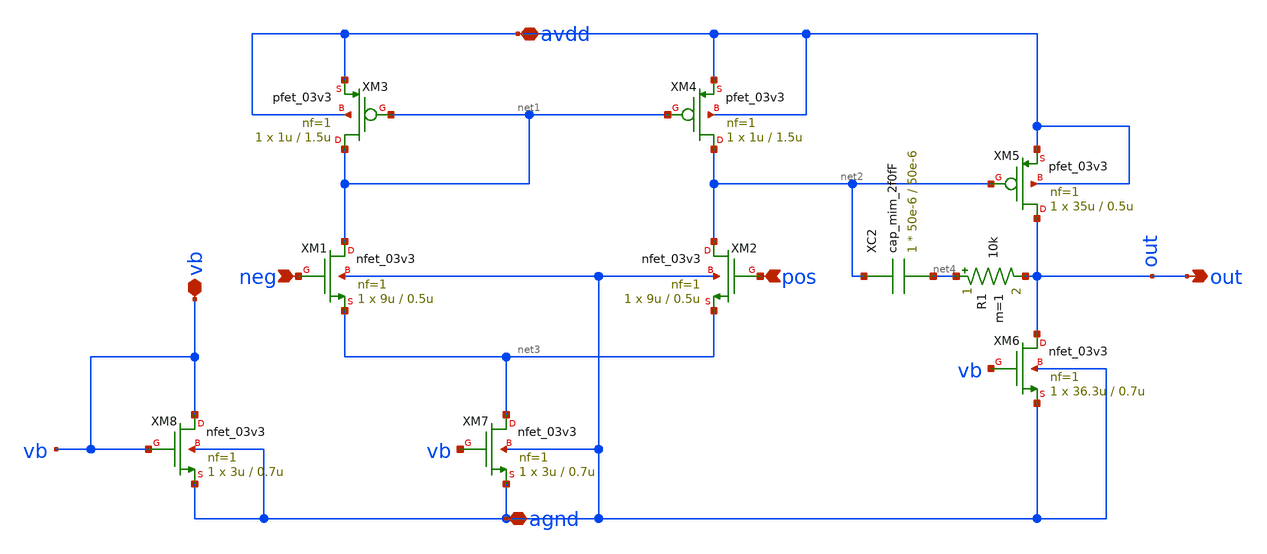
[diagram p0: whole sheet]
** sch_path: LDO/xschem/ota-ldo/symbol/ota-ldo.sch
**.subckt ota-ldo vb avdd agnd neg pos out
*.iopin vb
*.iopin avdd
*.iopin agnd
*.ipin neg
*.ipin pos
*.opin out
XC2 net2 net4 cap_mim_2f0fF c_width=50e-6 c_length=50e-6 m=1
XM1 net1 neg net3 agnd nfet_03v3 L=0.5u W=9u nf=1 ad='int((nf+1)/2) * W/nf * 0.18u' as='int((nf+2)/2) * W/nf * 0.18u'
+ pd='2*int((nf+1)/2) * (W/nf + 0.18u)' ps='2*int((nf+2)/2) * (W/nf + 0.18u)' nrd='0.18u / W' nrs='0.18u / W'
+ sa=0 sb=0 sd=0 m=1
XM3 net1 net1 avdd avdd pfet_03v3 L=1.5u W=1u nf=1 ad='int((nf+1)/2) * W/nf * 0.18u' as='int((nf+2)/2) * W/nf * 0.18u'
+ pd='2*int((nf+1)/2) * (W/nf + 0.18u)' ps='2*int((nf+2)/2) * (W/nf + 0.18u)' nrd='0.18u / W' nrs='0.18u / W'
+ sa=0 sb=0 sd=0 m=1
XM2 net2 pos net3 agnd nfet_03v3 L=0.5u W=9u nf=1 ad='int((nf+1)/2) * W/nf * 0.18u' as='int((nf+2)/2) * W/nf * 0.18u'
+ pd='2*int((nf+1)/2) * (W/nf + 0.18u)' ps='2*int((nf+2)/2) * (W/nf + 0.18u)' nrd='0.18u / W' nrs='0.18u / W'
+ sa=0 sb=0 sd=0 m=1
XM4 net2 net1 avdd avdd pfet_03v3 L=1.5u W=1u nf=1 ad='int((nf+1)/2) * W/nf * 0.18u' as='int((nf+2)/2) * W/nf * 0.18u'
+ pd='2*int((nf+1)/2) * (W/nf + 0.18u)' ps='2*int((nf+2)/2) * (W/nf + 0.18u)' nrd='0.18u / W' nrs='0.18u / W'
+ sa=0 sb=0 sd=0 m=1
XM7 net3 vb agnd agnd nfet_03v3 L=0.7u W=3u nf=1 ad='int((nf+1)/2) * W/nf * 0.18u' as='int((nf+2)/2) * W/nf * 0.18u'
+ pd='2*int((nf+1)/2) * (W/nf + 0.18u)' ps='2*int((nf+2)/2) * (W/nf + 0.18u)' nrd='0.18u / W' nrs='0.18u / W'
+ sa=0 sb=0 sd=0 m=1
XM8 vb vb agnd agnd nfet_03v3 L=0.7u W=3u nf=1 ad='int((nf+1)/2) * W/nf * 0.18u' as='int((nf+2)/2) * W/nf * 0.18u'
+ pd='2*int((nf+1)/2) * (W/nf + 0.18u)' ps='2*int((nf+2)/2) * (W/nf + 0.18u)' nrd='0.18u / W' nrs='0.18u / W'
+ sa=0 sb=0 sd=0 m=1
XM5 out net2 avdd avdd pfet_03v3 L=0.5u W=35u nf=1 ad='int((nf+1)/2) * W/nf * 0.18u' as='int((nf+2)/2) * W/nf * 0.18u'
+ pd='2*int((nf+1)/2) * (W/nf + 0.18u)' ps='2*int((nf+2)/2) * (W/nf + 0.18u)' nrd='0.18u / W' nrs='0.18u / W'
+ sa=0 sb=0 sd=0 m=1
XM6 out vb agnd agnd nfet_03v3 L=0.7u W=36.3u nf=1 ad='int((nf+1)/2) * W/nf * 0.18u' as='int((nf+2)/2) * W/nf * 0.18u'
+ pd='2*int((nf+1)/2) * (W/nf + 0.18u)' ps='2*int((nf+2)/2) * (W/nf + 0.18u)' nrd='0.18u / W' nrs='0.18u / W'
+ sa=0 sb=0 sd=0 m=1
R1 net4 out 10k m=1
**.ends
.end
